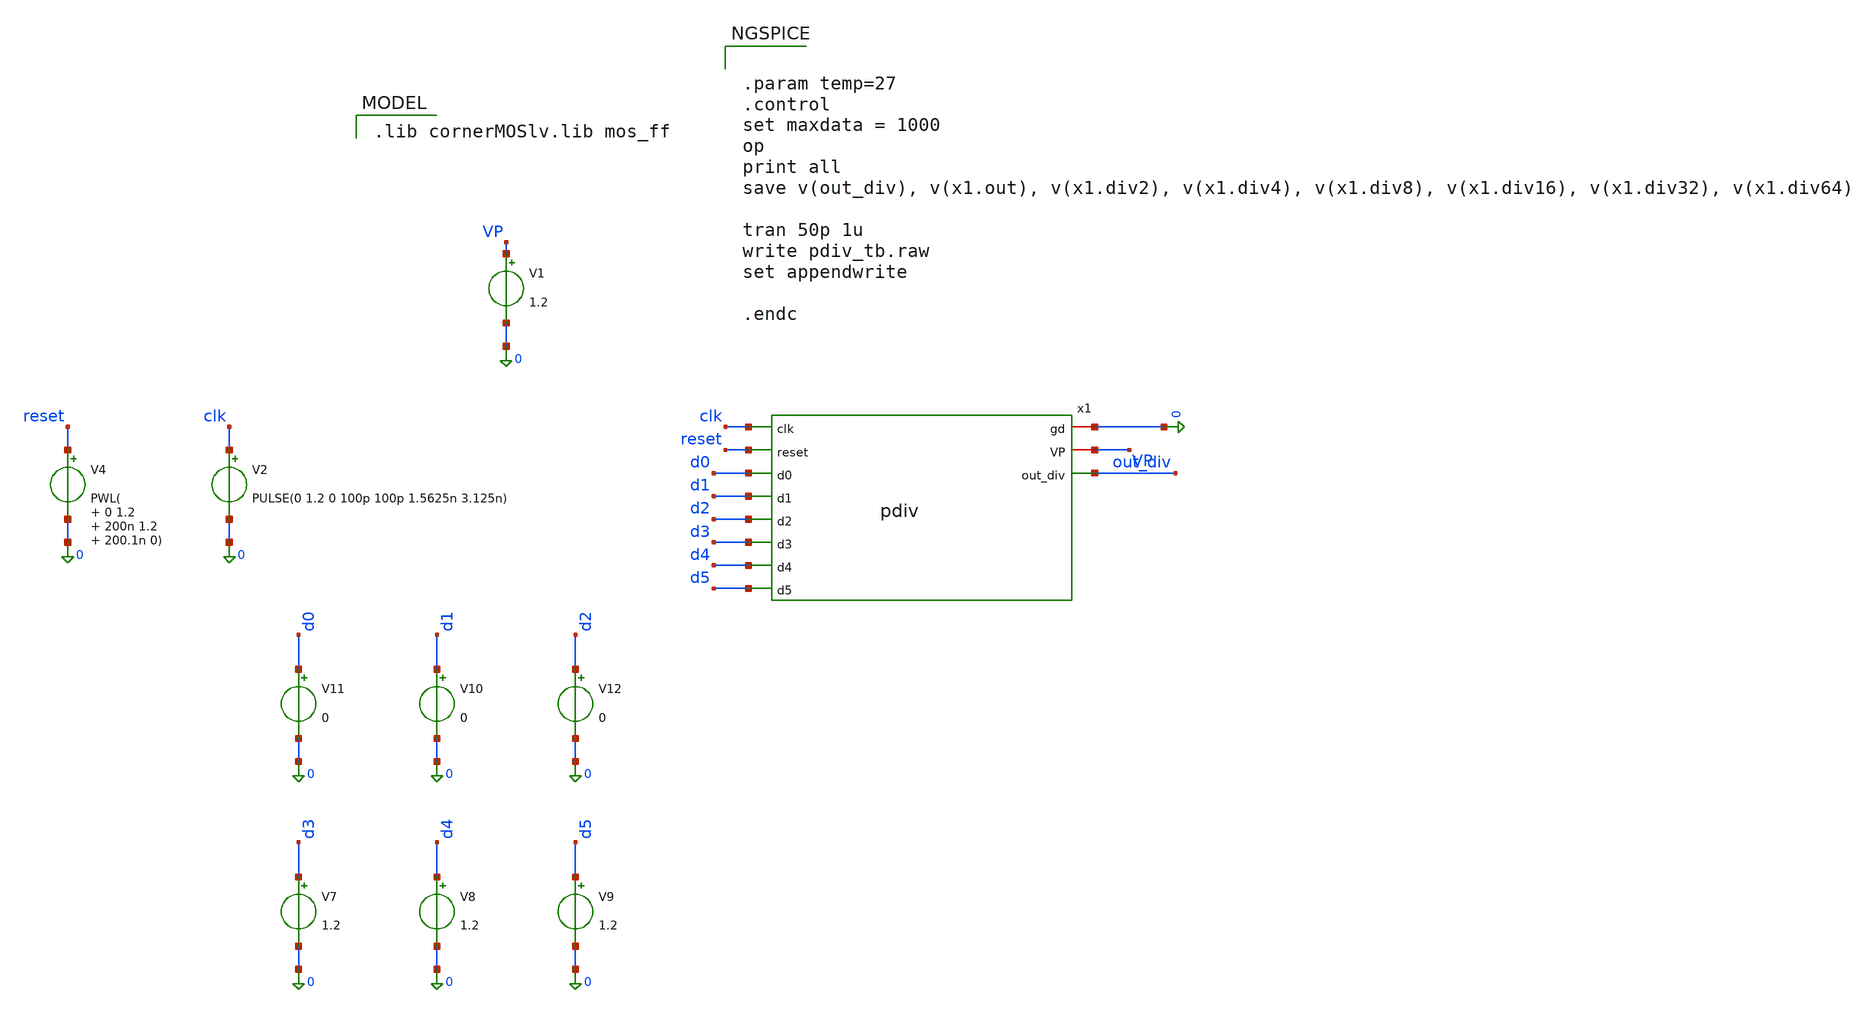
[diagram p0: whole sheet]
** sch_path: PLL0663-main/testbenches/tran/xschem/divider/pdiv_tb.sch
**.subckt pdiv_tb
V1 VP 0 1.2
V2 clk 0 PULSE(0 1.2 0 100p 100p 1.5625n 3.125n)
V8 d4 0 1.2
V9 d5 0 1.2
V11 d0 0 0
V10 d1 0 0
V12 d2 0 0
V7 d3 0 1.2
x1 0 VP clk reset d0 d1 d2 d3 d4 d5 out_div pdiv
V4 reset 0 PWL( 0 1.2 200n 1.2 200.1n 0)
**** begin user architecture code
 .lib cornerMOSlv.lib mos_ff



.param temp=27
.control
set maxdata = 1000
op
print all
save v(out_div), v(x1.out), v(x1.div2), v(x1.div4), v(x1.div8), v(x1.div16), v(x1.div32),
+ v(x1.div64)

tran 50p 1u
write pdiv_tb.raw
set appendwrite

.endc


**** end user architecture code
**.ends
.end
